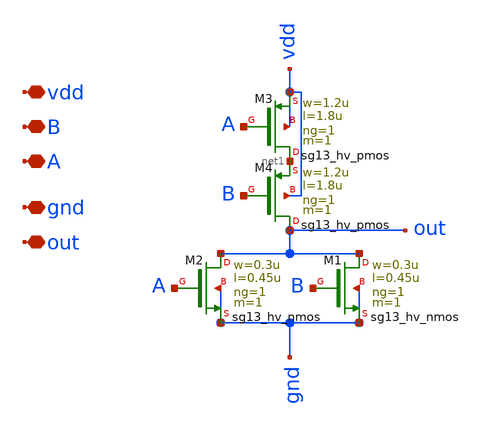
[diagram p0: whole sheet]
** sch_path: dependencies/OTA/dependencies/OTA5174-main/schematic/xschem/Clock_gen_using_transistor_hv/nor.sch
**.subckt nor vdd B A gnd out
*.iopin vdd
*.iopin B
*.iopin A
*.iopin gnd
*.iopin out
XM3 net1 A vdd vdd sg13_hv_pmos w=1.2u l=1.8u ng=1 m=1 mm_ok=1
XM1 out B gnd gnd sg13_hv_nmos w=0.3u l=0.45u ng=1 m=1 mm_ok=1
XM2 out A gnd gnd sg13_hv_nmos w=0.3u l=0.45u ng=1 m=1 mm_ok=1
XM4 out B net1 vdd sg13_hv_pmos w=1.2u l=1.8u ng=1 m=1 mm_ok=1
**.ends
.end
